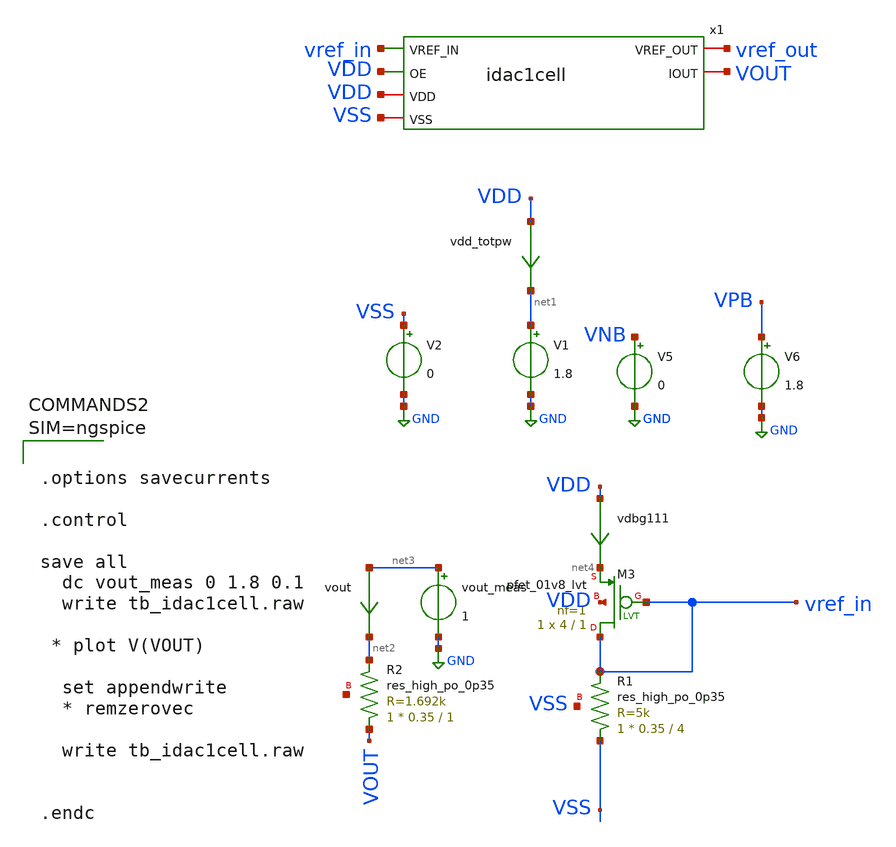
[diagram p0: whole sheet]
** sch_path: tt_um_emilian_rf_playground/xschem/tb_idac1cell.sch
**.subckt tb_idac1cell
V5 VNB GND 0
V6 VPB GND 1.8
V1 net1 GND 1.8
V2 VSS GND 0
XM3 vref_in vref_in net4 VDD sky130_fd_pr__pfet_01v8_lvt L=1 W=4 nf=1 ad='int((nf+1)/2) * W/nf * 0.29'
+ as='int((nf+2)/2) * W/nf * 0.29' pd='2*int((nf+1)/2) * (W/nf + 0.29)' ps='2*int((nf+2)/2) * (W/nf + 0.29)'
+ nrd='0.29 / W' nrs='0.29 / W' sa=0 sb=0 sd=0 mult=1 m=1
vout net3 net2 0
.save i(vout)
XR1 VSS vref_in VSS sky130_fd_pr__res_high_po_0p35 L=4 mult=1 m=1
vdbg111 VDD net4 0
.save i(vdbg111)
XR2 VOUT net2 net5 sky130_fd_pr__res_high_po_0p35 L=1 mult=1 m=1
x1 vref_in vref_out VOUT VDD VSS VDD idac1cell
vdd_totpw VDD net1 0
.save i(vdd_totpw)
vout_meas net3 GND 1
**** begin user architecture code

** opencircuitdesign pdks install
.lib $::SKYWATER_MODELS/sky130.lib.spice tt_mm
*.lib $::SKYWATER_STDCELLS/sky130_fd_sc_hd_blablabla.spice

.subckt sky130_fd_sc_hd__inv_1 A VGND VNB VPB VPWR Y
X0 VGND A Y VNB sky130_fd_pr__nfet_01v8 w=650000u l=150000u
X1 VPWR A Y VPB sky130_fd_pr__pfet_01v8_hvt w=1e+06u l=150000u
.ends





.options savecurrents

.control

save all
  dc vout_meas 0 1.8 0.1
  write tb_idac1cell.raw

 * plot V(VOUT)

  set appendwrite
  * remzerovec

  write tb_idac1cell.raw


.endc



**** end user architecture code
**.ends

* expanding   symbol:  idac1cell.sym # of pins=6
** sym_path: tt_um_emilian_rf_playground/xschem/idac1cell.sym
** sch_path: tt_um_emilian_rf_playground/xschem/idac1cell.sch
.subckt idac1cell VREF_IN VREF_OUT IOUT VDD VSS OE
*.ipin VSS
*.iopin VREF_OUT
*.ipin VREF_IN
*.iopin VDD
*.iopin IOUT
*.ipin OE
XM3 net1 net1 net2 net2 sky130_fd_pr__nfet_01v8_lvt L=1 W=2 nf=1 ad='int((nf+1)/2) * W/nf * 0.29' as='int((nf+2)/2) * W/nf * 0.29'
+ pd='2*int((nf+1)/2) * (W/nf + 0.29)' ps='2*int((nf+2)/2) * (W/nf + 0.29)' nrd='0.29 / W' nrs='0.29 / W'
+ sa=0 sb=0 sd=0 mult=1 m=1
XM4 net1 net1 VSS VSS sky130_fd_pr__nfet_01v8_lvt L=1 W=2 nf=1 ad='int((nf+1)/2) * W/nf * 0.29' as='int((nf+2)/2) * W/nf * 0.29'
+ pd='2*int((nf+1)/2) * (W/nf + 0.29)' ps='2*int((nf+2)/2) * (W/nf + 0.29)' nrd='0.29 / W' nrs='0.29 / W'
+ sa=0 sb=0 sd=0 mult=1 m=1
XM1 net1 VREF_IN VDD VDD sky130_fd_pr__pfet_01v8_lvt L=1 W=4 nf=1 ad='int((nf+1)/2) * W/nf * 0.29' as='int((nf+2)/2) * W/nf * 0.29'
+ pd='2*int((nf+1)/2) * (W/nf + 0.29)' ps='2*int((nf+2)/2) * (W/nf + 0.29)' nrd='0.29 / W' nrs='0.29 / W'
+ sa=0 sb=0 sd=0 mult=1 m=1
XM5 net3 net1 VSS VSS sky130_fd_pr__nfet_01v8_lvt L=1 W=2 nf=1 ad='int((nf+1)/2) * W/nf * 0.29' as='int((nf+2)/2) * W/nf * 0.29'
+ pd='2*int((nf+1)/2) * (W/nf + 0.29)' ps='2*int((nf+2)/2) * (W/nf + 0.29)' nrd='0.29 / W' nrs='0.29 / W'
+ sa=0 sb=0 sd=0 mult=1 m=1
XM2 VREF_OUT VREF_OUT VDD VDD sky130_fd_pr__pfet_01v8_lvt L=1 W=4 nf=1 ad='int((nf+1)/2) * W/nf * 0.29'
+ as='int((nf+2)/2) * W/nf * 0.29' pd='2*int((nf+1)/2) * (W/nf + 0.29)' ps='2*int((nf+2)/2) * (W/nf + 0.29)'
+ nrd='0.29 / W' nrs='0.29 / W' sa=0 sb=0 sd=0 mult=1 m=1
XM6 vdrain2 net1 VSS VSS sky130_fd_pr__nfet_01v8_lvt L=1 W=2 nf=1 ad='int((nf+1)/2) * W/nf * 0.29' as='int((nf+2)/2) * W/nf * 0.29'
+ pd='2*int((nf+1)/2) * (W/nf + 0.29)' ps='2*int((nf+2)/2) * (W/nf + 0.29)' nrd='0.29 / W' nrs='0.29 / W'
+ sa=0 sb=0 sd=0 mult=1 m=1
XM7 net4 OE vdrain2 VSS sky130_fd_pr__nfet_01v8_lvt L=1 W=2 nf=1 ad='int((nf+1)/2) * W/nf * 0.29' as='int((nf+2)/2) * W/nf * 0.29'
+ pd='2*int((nf+1)/2) * (W/nf + 0.29)' ps='2*int((nf+2)/2) * (W/nf + 0.29)' nrd='0.29 / W' nrs='0.29 / W'
+ sa=0 sb=0 sd=0 mult=1 m=1
vmeas VREF_OUT net3 0
.save i(vmeas)
viout IOUT net4 0
.save i(viout)
vref net2 VSS 0
.save i(vref)
.ends

.GLOBAL GND
.end
